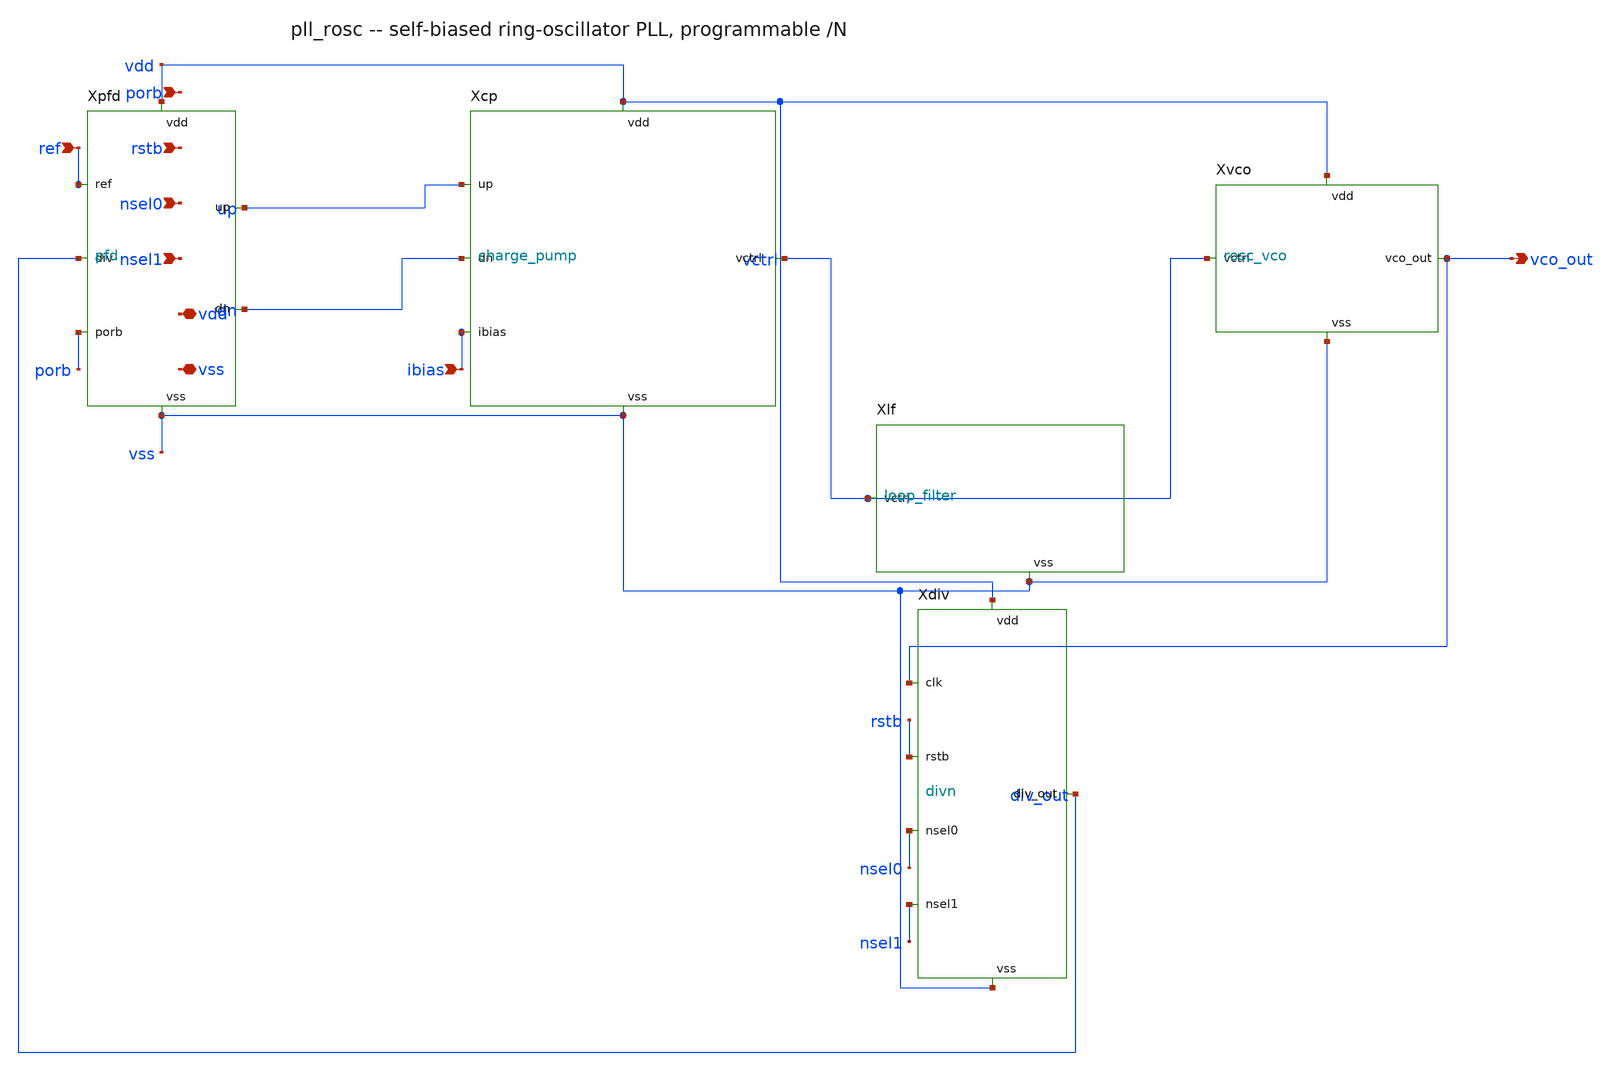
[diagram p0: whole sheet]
** sch_path: xschem/pll_rosc_wired.sch
**.subckt pll_rosc_wired ref porb rstb nsel0 nsel1 ibias vco_out vdd vss
*.ipin ref
*.ipin porb
*.ipin rstb
*.ipin nsel0
*.ipin nsel1
*.ipin ibias
*.opin vco_out
*.iopin vdd
*.iopin vss
Xpfd ref div_out porb up dn vdd vss pfd
Xcp up dn ibias vctrl vdd vss charge_pump
Xlf vctrl vss loop_filter
Xvco vctrl vco_out vdd vss rosc_vco
Xdiv vco_out rstb nsel0 nsel1 div_out vdd vss divn
**.ends

* expanding   symbol:  pfd.sym # of pins=7
** sym_path: xschem/pfd.sym
** sch_path: xschem/pfd.sch
.subckt pfd ref div porb up dn vdd vss
*.ipin ref
*.ipin div
*.ipin porb
*.opin up
*.opin dn
*.iopin vdd
*.iopin vss
Xup up upn ref dhi rstb vdd vss sg13cmos5l_dfrbp_1
Xdn dn dnn div dhi rstb vdd vss sg13cmos5l_dfrbp_1
Xtiehi dhi vdd vss sg13cmos5l_tiehi
Xnand nout up dn vdd vss sg13cmos5l_nand2_1
Xand rstb nout porb vdd vss sg13cmos5l_and2_1
Xantref ref vdd vss sg13cmos5l_antennanp
Xantporb porb vdd vss sg13cmos5l_antennanp
.ends


* expanding   symbol:  charge_pump.sym # of pins=6
** sym_path: xschem/charge_pump.sym
** sch_path: xschem/charge_pump.sch
.subckt charge_pump up dn ibias vctrl vdd vss
*.ipin up
*.ipin dn
*.ipin ibias
*.iopin vctrl
*.iopin vdd
*.iopin vss
XMn0 ibias ibias vss vss sg13_lv_nmos w=2u l=0.5u ng=1 m=1 mm_ok=1
XMn1 vbp ibias vss vss sg13_lv_nmos w=2u l=0.5u ng=1 m=1 mm_ok=1
XMp0 vbp vbp vdd vdd sg13_lv_pmos w=4u l=0.5u ng=1 m=1 mm_ok=1
XMpsrc a vbp vdd vdd sg13_lv_pmos w=4u l=0.5u ng=1 m=1 mm_ok=1
XMnsnk b ibias vss vss sg13_lv_nmos w=2u l=0.5u ng=1 m=1 mm_ok=1
XMpi upb up vdd vdd sg13_lv_pmos w=2u l=0.13u ng=1 m=1 mm_ok=1
XMni upb up vss vss sg13_lv_nmos w=1u l=0.13u ng=1 m=1 mm_ok=1
XMswup vctrl upb a vdd sg13_lv_pmos w=4u l=0.13u ng=1 m=1 mm_ok=1
XMswdn vctrl dn b vss sg13_lv_nmos w=2u l=0.13u ng=1 m=1 mm_ok=1
.ends


* expanding   symbol:  loop_filter.sym # of pins=2
** sym_path: xschem/loop_filter.sym
** sch_path: xschem/loop_filter.sch
.subckt loop_filter vctrl vss
*.iopin vctrl
*.iopin vss
XRz vctrl nz sub! rhigh w=1u l=88u m=1 b=0 mm_ok=1
XCz nz vss cap_cmomf w=82u l=82u mmin=1 mmax=4 subblock=0 rfmodel=0 subscale=1 m=1 mm_ok=1
XCp vctrl vss cap_cmomf w=16u l=16u mmin=1 mmax=4 subblock=0 rfmodel=0 subscale=1 m=1 mm_ok=1
.ends


* expanding   symbol:  rosc_vco.sym # of pins=4
** sym_path: xschem/rosc_vco.sym
** sch_path: xschem/rosc_vco.sch
.subckt rosc_vco vctrl vco_out vdd vss
*.ipin vctrl
*.opin vco_out
*.iopin vdd
*.iopin vss
XMpr vbp vbp vdd vdd sg13_lv_pmos w=1u l=0.13u ng=1 m=1 mm_ok=1
XMnr vbp vctrl vss vss sg13_lv_nmos w=1u l=0.13u ng=1 m=1 mm_ok=1
X1 n1 n2 vdd vbp vctrl vss cs_inv
X2 n2 n3 vdd vbp vctrl vss cs_inv
X3 n3 n4 vdd vbp vctrl vss cs_inv
X4 n4 n5 vdd vbp vctrl vss cs_inv
X5 n5 n6 vdd vbp vctrl vss cs_inv
X6 n6 n7 vdd vbp vctrl vss cs_inv
X7 n7 n1 vdd vbp vctrl vss cs_inv
Xtap vco_outn n1 vdd vss sg13cmos5l_inv_1
Xbuf vco_out vco_outn vdd vss sg13cmos5l_inv_4
Xdum2 ndum2 n2 vdd vss sg13cmos5l_inv_1
Xdum3 ndum3 n3 vdd vss sg13cmos5l_inv_1
Xdum4 ndum4 n4 vdd vss sg13cmos5l_inv_1
Xdum5 ndum5 n5 vdd vss sg13cmos5l_inv_1
Xdum6 ndum6 n6 vdd vss sg13cmos5l_inv_1
Xdum7 ndum7 n7 vdd vss sg13cmos5l_inv_1
.ends


* expanding   symbol:  divn.sym # of pins=7
** sym_path: xschem/divn.sym
** sch_path: xschem/divn.sch
.subckt divn clk rstb nsel0 nsel1 div_out vdd vss
*.ipin clk
*.ipin rstb
*.ipin nsel0
*.ipin nsel1
*.opin div_out
*.iopin vdd
*.iopin vss
Xd1 q1 q1b clk q1b rstb vdd vss sg13cmos5l_dfrbp_1
Xd2 q2 q2b q1 q2b rstb vdd vss sg13cmos5l_dfrbp_1
Xd3 q3 q3b q2 q3b rstb vdd vss sg13cmos5l_dfrbp_1
Xd4 q4 q4b q3 q4b rstb vdd vss sg13cmos5l_dfrbp_1
Xmux div_out q1 q2 q3 q4 nsel0 nsel1 vdd vss sg13cmos5l_mux4_1
.ends


* expanding   symbol:  cs_inv.sym # of pins=6
** sym_path: xschem/cs_inv.sym
** sch_path: xschem/cs_inv.sch
.subckt cs_inv in out vdd vbp vctrl vss
*.ipin in
*.opin out
*.ipin vbp
*.ipin vctrl
*.iopin vdd
*.iopin vss
XMps nph vbp vdd vdd sg13_lv_pmos w=1u l=0.13u ng=1 m=1 mm_ok=1
XMpu out in nph vdd sg13_lv_pmos w=2u l=0.13u ng=1 m=1 mm_ok=1
XMnd out in npl vss sg13_lv_nmos w=2u l=0.13u ng=1 m=1 mm_ok=1
XMns npl vctrl vss vss sg13_lv_nmos w=1u l=0.13u ng=1 m=1 mm_ok=1
.ends

.end
